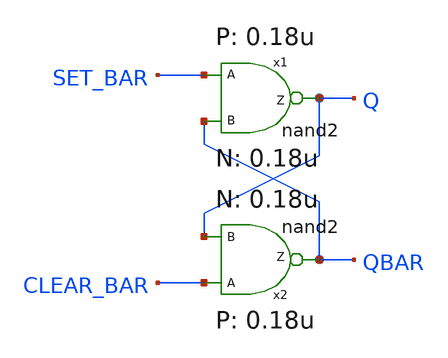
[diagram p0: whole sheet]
** sch_path: xschem_library/mylib/test.sch
**.subckt test
x1 Q SET_BAR QBAR nand2 WP=8u LP=0.18u WN=5u LN=0.18u
x2 QBAR CLEAR_BAR Q nand2 WP=8u LP=0.18u WN=5u LN=0.18u
**.ends

* expanding   symbol:  mylib/nand2.sym # of pins=3
** sym_path: library/mylib/nand2.sym
** sch_path: library/mylib/nand2.sch
.subckt nand2 Z A B  WP=8u LP=0.18u WN=5u LN=0.18u
*.ipin A
*.opin Z
*.ipin B
m1 Z A net1 VSS nmos w=WN l=LN m=1
m2 Z B VCC VCC pmos w=WP l=LP m=1
m3 Z A VCC VCC pmos w=WP l=LP m=1
m4 net1 B VSS VSS nmos w=WN l=LN m=1
.ends

.GLOBAL VCC
.GLOBAL VSS
.end
